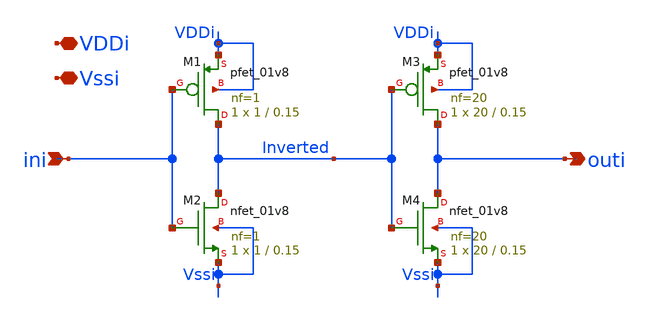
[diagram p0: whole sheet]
** sch_path: xschem/double_inverter.sch
**.subckt double_inverter VDDi Vssi outi ini
*.iopin VDDi
*.iopin Vssi
*.opin outi
*.ipin ini
XM1 Inverted ini VDDi VDDi sky130_fd_pr__pfet_01v8 L=0.15 W=1 nf=1 ad='int((nf+1)/2) * W/nf * 0.29' as='int((nf+2)/2) * W/nf * 0.29'
+ pd='2*int((nf+1)/2) * (W/nf + 0.29)' ps='2*int((nf+2)/2) * (W/nf + 0.29)' nrd='0.29 / W' nrs='0.29 / W'
+ sa=0 sb=0 sd=0 mult=1 m=1
XM2 Inverted ini Vssi Vssi sky130_fd_pr__nfet_01v8 L=0.15 W=1 nf=1 ad='int((nf+1)/2) * W/nf * 0.29' as='int((nf+2)/2) * W/nf * 0.29'
+ pd='2*int((nf+1)/2) * (W/nf + 0.29)' ps='2*int((nf+2)/2) * (W/nf + 0.29)' nrd='0.29 / W' nrs='0.29 / W'
+ sa=0 sb=0 sd=0 mult=1 m=1
XM3 outi Inverted VDDi VDDi sky130_fd_pr__pfet_01v8 L=0.15 W=20 nf=20 ad='int((nf+1)/2) * W/nf * 0.29'
+ as='int((nf+2)/2) * W/nf * 0.29' pd='2*int((nf+1)/2) * (W/nf + 0.29)' ps='2*int((nf+2)/2) * (W/nf + 0.29)'
+ nrd='0.29 / W' nrs='0.29 / W' sa=0 sb=0 sd=0 mult=1 m=1
XM4 outi Inverted Vssi Vssi sky130_fd_pr__nfet_01v8 L=0.15 W=20 nf=20 ad='int((nf+1)/2) * W/nf * 0.29'
+ as='int((nf+2)/2) * W/nf * 0.29' pd='2*int((nf+1)/2) * (W/nf + 0.29)' ps='2*int((nf+2)/2) * (W/nf + 0.29)'
+ nrd='0.29 / W' nrs='0.29 / W' sa=0 sb=0 sd=0 mult=1 m=1
**.ends
.end
